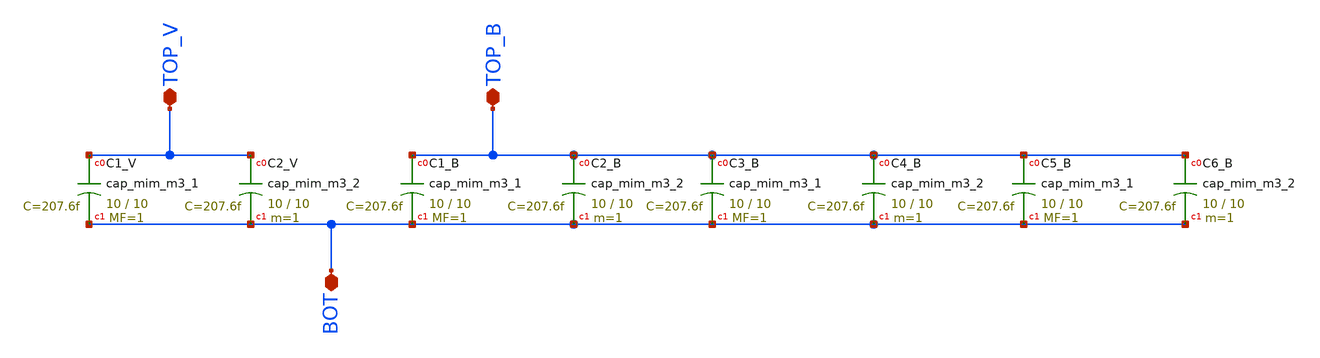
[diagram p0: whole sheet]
** sch_path: modules/CAPOSC/symbol/CAPOSC.sch
**.subckt CAPOSC TOP_V TOP_B BOT
*.iopin TOP_V
*.iopin TOP_B
*.iopin BOT
XC1_V TOP_V BOT sky130_fd_pr__cap_mim_m3_1 W=10 L=10 MF=1 m=1
XC2_V TOP_V BOT sky130_fd_pr__cap_mim_m3_2 W=10 L=10 MF=1 m=1
XC1_B TOP_B BOT sky130_fd_pr__cap_mim_m3_1 W=10 L=10 MF=1 m=1
XC2_B TOP_B BOT sky130_fd_pr__cap_mim_m3_2 W=10 L=10 MF=1 m=1
XC5_B TOP_B BOT sky130_fd_pr__cap_mim_m3_1 W=10 L=10 MF=1 m=1
XC6_B TOP_B BOT sky130_fd_pr__cap_mim_m3_2 W=10 L=10 MF=1 m=1
XC3_B TOP_B BOT sky130_fd_pr__cap_mim_m3_1 W=10 L=10 MF=1 m=1
XC4_B TOP_B BOT sky130_fd_pr__cap_mim_m3_2 W=10 L=10 MF=1 m=1
**.ends
.end
